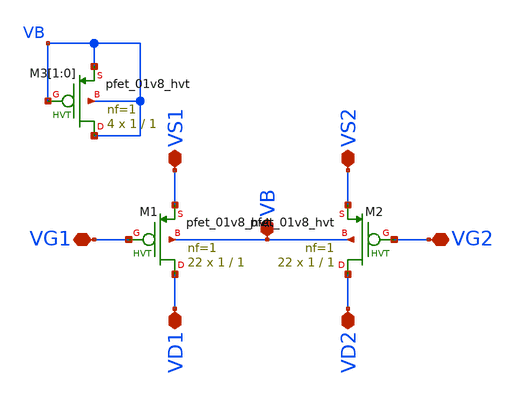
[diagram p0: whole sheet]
** sch_path: xschem/INA_layout_v2/pfets.sch
**.subckt pfets VS1 VS2 VB VG1 VG2 VD1 VD2
*.iopin VS1
*.iopin VS2
*.iopin VB
*.iopin VG1
*.iopin VG2
*.iopin VD1
*.iopin VD2
XM1 VD1 VG1 VS1 VB sky130_fd_pr__pfet_01v8_hvt L=1 W=1 nf=1 ad='int((nf+1)/2) * W/nf * 0.29' as='int((nf+2)/2) * W/nf * 0.29'
+ pd='2*int((nf+1)/2) * (W/nf + 0.29)' ps='2*int((nf+2)/2) * (W/nf + 0.29)' nrd='0.29 / W' nrs='0.29 / W'
+ sa=0 sb=0 sd=0 mult=22 m=22
XM2 VD2 VG2 VS2 VB sky130_fd_pr__pfet_01v8_hvt L=1 W=1 nf=1 ad='int((nf+1)/2) * W/nf * 0.29' as='int((nf+2)/2) * W/nf * 0.29'
+ pd='2*int((nf+1)/2) * (W/nf + 0.29)' ps='2*int((nf+2)/2) * (W/nf + 0.29)' nrd='0.29 / W' nrs='0.29 / W'
+ sa=0 sb=0 sd=0 mult=22 m=22
XM3[1] VB VB VB VB sky130_fd_pr__pfet_01v8_hvt L=1 W=1 nf=1 ad='int((nf+1)/2) * W/nf * 0.29' as='int((nf+2)/2) * W/nf * 0.29'
+ pd='2*int((nf+1)/2) * (W/nf + 0.29)' ps='2*int((nf+2)/2) * (W/nf + 0.29)' nrd='0.29 / W' nrs='0.29 / W'
+ sa=0 sb=0 sd=0 mult=4 m=4
XM3[0] VB VB VB VB sky130_fd_pr__pfet_01v8_hvt L=1 W=1 nf=1 ad='int((nf+1)/2) * W/nf * 0.29' as='int((nf+2)/2) * W/nf * 0.29'
+ pd='2*int((nf+1)/2) * (W/nf + 0.29)' ps='2*int((nf+2)/2) * (W/nf + 0.29)' nrd='0.29 / W' nrs='0.29 / W'
+ sa=0 sb=0 sd=0 mult=4 m=4
**.ends
.end
